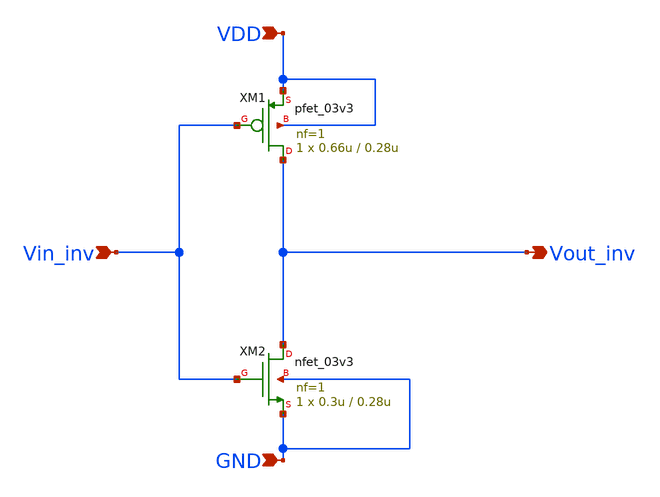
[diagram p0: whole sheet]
** sch_path: blocks/adc/lvds/inverter_chain.sch
**.subckt inverter_chain Vin_inv Vout_inv VDD GND
*.ipin Vin_inv
*.opin Vout_inv
*.ipin VDD
*.ipin GND
XM1 Vout_inv Vin_inv VDD VDD pfet_03v3 L=0.28u W=0.66u nf=1 ad='int((nf+1)/2) * W/nf * 0.18u' as='int((nf+2)/2) * W/nf * 0.18u'
+ pd='2*int((nf+1)/2) * (W/nf + 0.18u)' ps='2*int((nf+2)/2) * (W/nf + 0.18u)' nrd='0.18u / W' nrs='0.18u / W'
+ sa=0 sb=0 sd=0 m=1
XM2 Vout_inv Vin_inv GND GND nfet_03v3 L=0.28u W=0.3u nf=1 ad='int((nf+1)/2) * W/nf * 0.18u' as='int((nf+2)/2) * W/nf * 0.18u'
+ pd='2*int((nf+1)/2) * (W/nf + 0.18u)' ps='2*int((nf+2)/2) * (W/nf + 0.18u)' nrd='0.18u / W' nrs='0.18u / W'
+ sa=0 sb=0 sd=0 m=1
**.ends
.end
